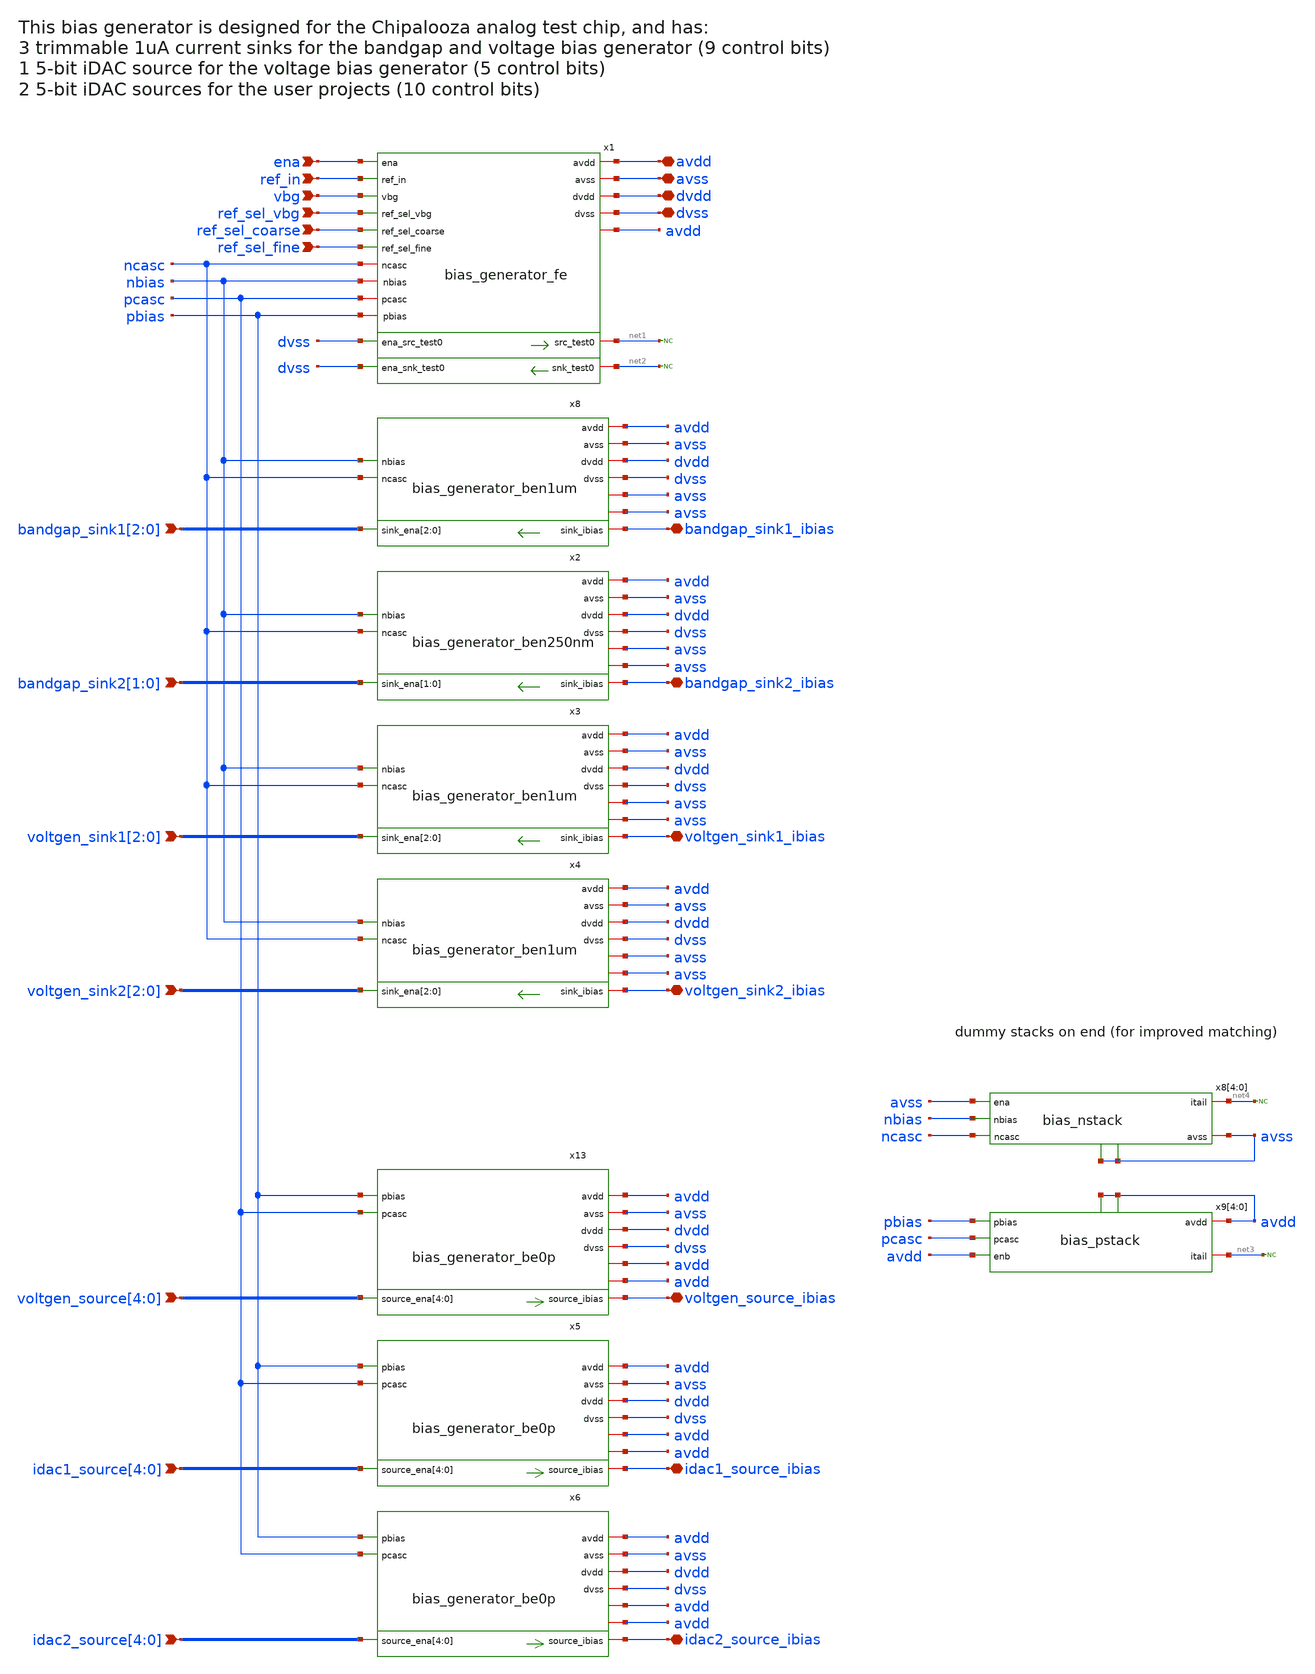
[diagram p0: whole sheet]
** sch_path: projects/programmable_transceiver_platform/analog/core_support/biasgen/xschem/gf180mcu_ocd_ip__biasgen.sch
**.subckt gf180mcu_ocd_ip__biasgen avdd avss dvdd dvss ena ref_in vbg ref_sel_vbg
*+ bandgap_sink1[2],bandgap_sink1[1],bandgap_sink1[0] voltgen_sink1[2],voltgen_sink1[1],voltgen_sink1[0]
*+ voltgen_sink2[2],voltgen_sink2[1],voltgen_sink2[0] bandgap_sink1_ibias voltgen_sink1_ibias voltgen_sink2_ibias ref_sel_fine ref_sel_coarse
*+ voltgen_source_ibias voltgen_source[4],voltgen_source[3],voltgen_source[2],voltgen_source[1],voltgen_source[0]
*+ bandgap_sink2[1],bandgap_sink2[0] bandgap_sink2_ibias idac1_source_ibias
*+ idac1_source[4],idac1_source[3],idac1_source[2],idac1_source[1],idac1_source[0] idac2_source_ibias idac2_source[4],idac2_source[3],idac2_source[2],idac2_source[1],idac2_source[0]
*.iopin avdd
*.iopin avss
*.iopin dvdd
*.iopin dvss
*.ipin ena
*.ipin ref_in
*.ipin vbg
*.ipin ref_sel_vbg
*.ipin bandgap_sink1[2],bandgap_sink1[1],bandgap_sink1[0]
*.ipin voltgen_sink1[2],voltgen_sink1[1],voltgen_sink1[0]
*.ipin voltgen_sink2[2],voltgen_sink2[1],voltgen_sink2[0]
*.iopin bandgap_sink1_ibias
*.iopin voltgen_sink1_ibias
*.iopin voltgen_sink2_ibias
*.ipin ref_sel_fine
*.ipin ref_sel_coarse
*.iopin voltgen_source_ibias
*.ipin voltgen_source[4],voltgen_source[3],voltgen_source[2],voltgen_source[1],voltgen_source[0]
*.ipin bandgap_sink2[1],bandgap_sink2[0]
*.iopin bandgap_sink2_ibias
*.iopin idac1_source_ibias
*.ipin idac1_source[4],idac1_source[3],idac1_source[2],idac1_source[1],idac1_source[0]
*.iopin idac2_source_ibias
*.ipin idac2_source[4],idac2_source[3],idac2_source[2],idac2_source[1],idac2_source[0]
x1 avdd ena vbg net1 avss dvdd dvss ref_sel_vbg ref_in dvss nbias pcasc pbias net2 dvss ncasc
+ ref_sel_fine ref_sel_coarse avdd bias_generator_fe
* noconn #net1
* noconn #net2
x13 dvdd dvss avdd pcasc pbias voltgen_source[4] voltgen_source[3] voltgen_source[2]
+ voltgen_source[1] voltgen_source[0] voltgen_source_ibias avss avdd avdd bias_generator_be0p
x8[4] net4 avss ncasc nbias avss avss avss bias_nstack
x8[3] net4 avss ncasc nbias avss avss avss bias_nstack
x8[2] net4 avss ncasc nbias avss avss avss bias_nstack
x8[1] net4 avss ncasc nbias avss avss avss bias_nstack
x8[0] net4 avss ncasc nbias avss avss avss bias_nstack
x9[4] avdd pbias pcasc avdd net3 avdd avdd bias_pstack
x9[3] avdd pbias pcasc avdd net3 avdd avdd bias_pstack
x9[2] avdd pbias pcasc avdd net3 avdd avdd bias_pstack
x9[1] avdd pbias pcasc avdd net3 avdd avdd bias_pstack
x9[0] avdd pbias pcasc avdd net3 avdd avdd bias_pstack
* noconn #net4
* noconn #net3
x8 dvdd dvss avdd nbias avss bandgap_sink1[2] bandgap_sink1[1] bandgap_sink1[0] bandgap_sink1_ibias
+ ncasc avss avss bias_generator_ben1um
x3 dvdd dvss avdd nbias avss voltgen_sink1[2] voltgen_sink1[1] voltgen_sink1[0] voltgen_sink1_ibias
+ ncasc avss avss bias_generator_ben1um
x4 dvdd dvss avdd nbias avss voltgen_sink2[2] voltgen_sink2[1] voltgen_sink2[0] voltgen_sink2_ibias
+ ncasc avss avss bias_generator_ben1um
x2 dvdd dvss avdd nbias avss bandgap_sink2[1] bandgap_sink2[0] bandgap_sink2_ibias ncasc avss avss
+ bias_generator_ben250nm
x5 dvdd dvss avdd pcasc pbias idac1_source[4] idac1_source[3] idac1_source[2] idac1_source[1]
+ idac1_source[0] idac1_source_ibias avss avdd avdd bias_generator_be0p
x6 dvdd dvss avdd pcasc pbias idac2_source[4] idac2_source[3] idac2_source[2] idac2_source[1]
+ idac2_source[0] idac2_source_ibias avss avdd avdd bias_generator_be0p
**.ends
.end
